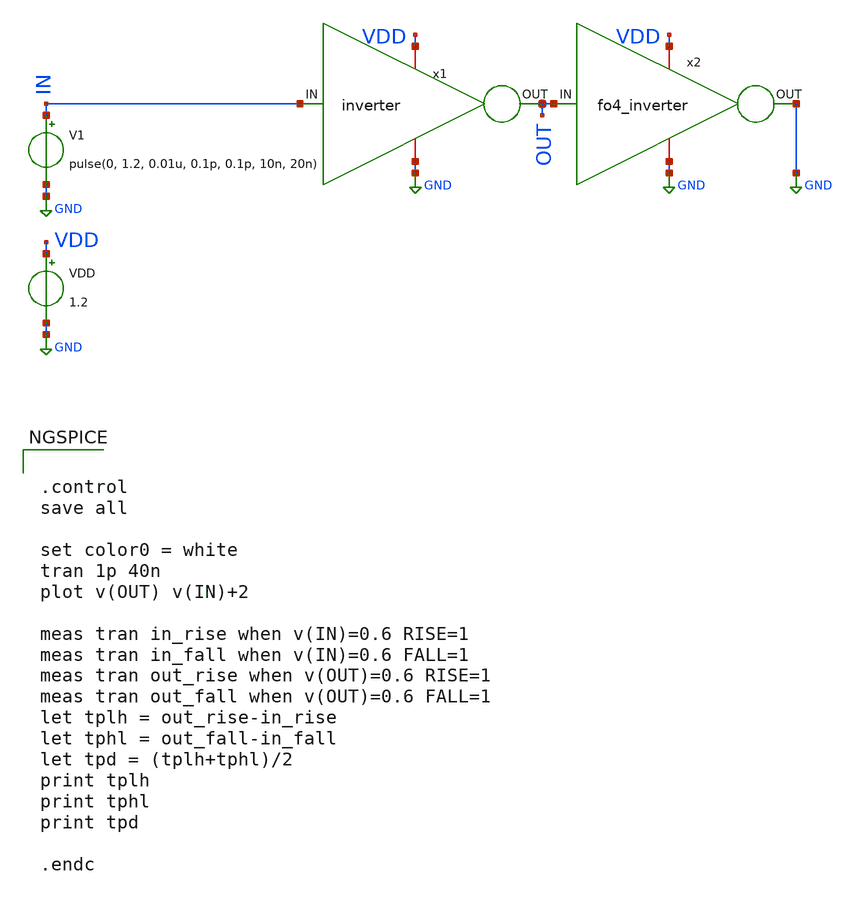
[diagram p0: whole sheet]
** sch_path: design/inv_with_fo4/inverter_tb.sch
**.subckt inverter_tb
x1 IN VDD OUT GND inverter
VDD VDD GND 1.2
V1 IN GND pulse(0, 1.2, 0.01u, 0.1p, 0.1p, 10n, 20n)
x2 VDD OUT GND GND fo4_inverter
**** begin user architecture code

** opencircuitdesign pdks install
.lib $::SKYWATER_MODELS/sky130.lib.spice tt_mm




.control
save all

set color0 = white
tran 1p 40n
plot v(OUT) v(IN)+2

meas tran in_rise when v(IN)=0.6 RISE=1
meas tran in_fall when v(IN)=0.6 FALL=1
meas tran out_rise when v(OUT)=0.6 RISE=1
meas tran out_fall when v(OUT)=0.6 FALL=1
let tplh = out_rise-in_rise
let tphl = out_fall-in_fall
let tpd = (tplh+tphl)/2
print tplh
print tphl
print tpd

.endc

**** end user architecture code
**.ends

* expanding   symbol:  inverter.sym # of pins=4
** sym_path: design/inv_with_fo4/inverter.sym
** sch_path: design/inv_with_fo4/inverter.sch
.subckt inverter IN VDD OUT VSS
*.ipin IN
*.iopin VDD
*.opin OUT
*.iopin VSS
XM2 OUT IN VDD VDD sky130_fd_pr__pfet_01v8 L=0.15 W=1.732 nf=1 ad='int((nf+1)/2) * W/nf * 0.29' as='int((nf+2)/2) * W/nf * 0.29'
+ pd='2*int((nf+1)/2) * (W/nf + 0.29)' ps='2*int((nf+2)/2) * (W/nf + 0.29)' nrd='0.29 / W' nrs='0.29 / W'
+ sa=0 sb=0 sd=0 mult=1 m=1
XM1 OUT IN VSS VSS sky130_fd_pr__nfet_01v8 L=0.15 W=1 nf=1 ad='int((1 + 1)/2) * 1 / 1 * 0.29' as='int((1 + 2)/2) * 1 / 1 * 0.29'
+ pd='2*int((1 + 1)/2) * (1 / 1 + 0.29)' ps='2*int((1 + 2)/2) * (1 / 1 + 0.29)' nrd='0.29 / 1 ' nrs='0.29 / 1 '
+ sa=0 sb=0 sd=0 mult=1 m=1
.ends


* expanding   symbol:  fo4_inverter.sym # of pins=4
** sym_path: design/2x1_mux_with_fo4/fo4_inverter.sym
** sch_path: design/2x1_mux_with_fo4/fo4_inverter.sch
.subckt fo4_inverter VDD IN OUT VSS
*.ipin IN
*.iopin VDD
*.iopin VSS
*.opin OUT
x1 VDD OUT IN VSS inverter
x2 VDD OUT IN VSS inverter
x3 VDD OUT IN VSS inverter
x4 VDD OUT IN VSS inverter
.ends

.GLOBAL GND
.end
